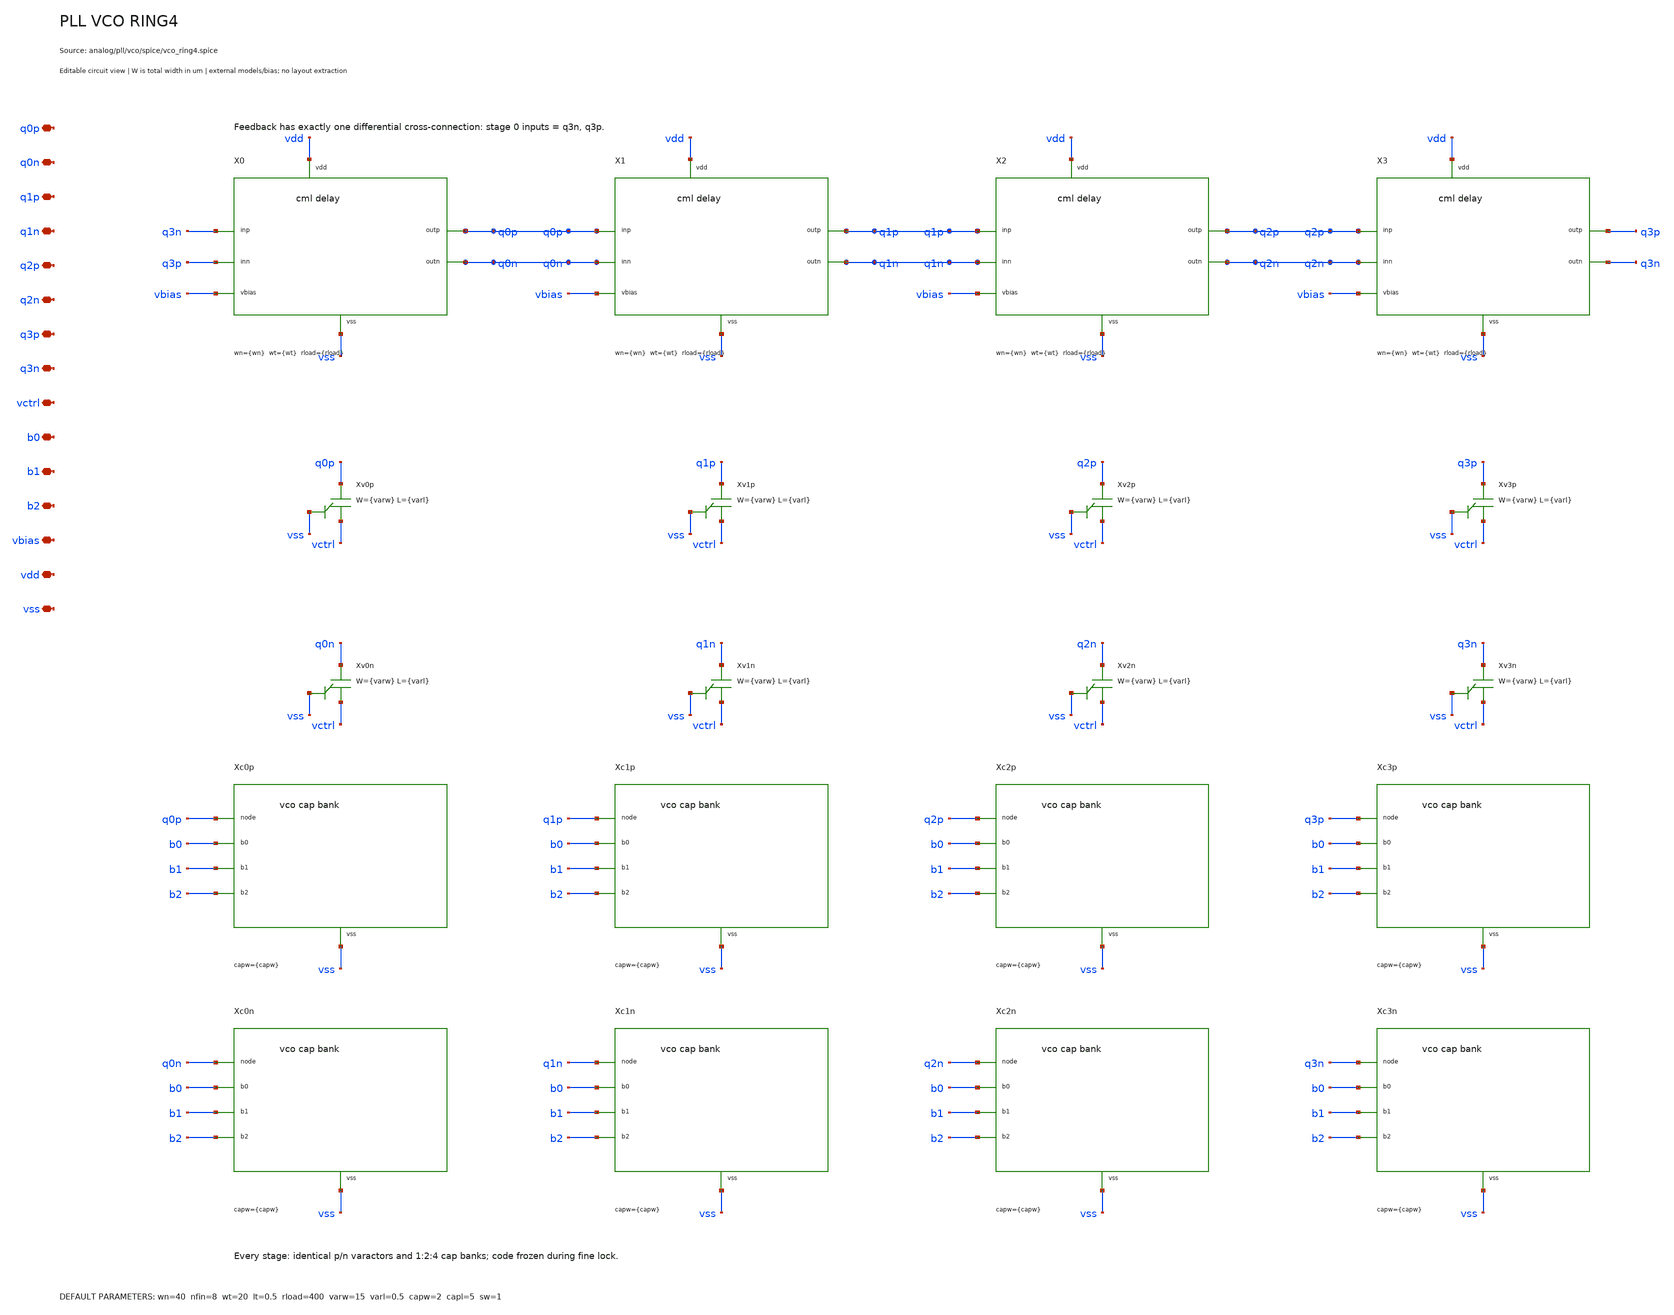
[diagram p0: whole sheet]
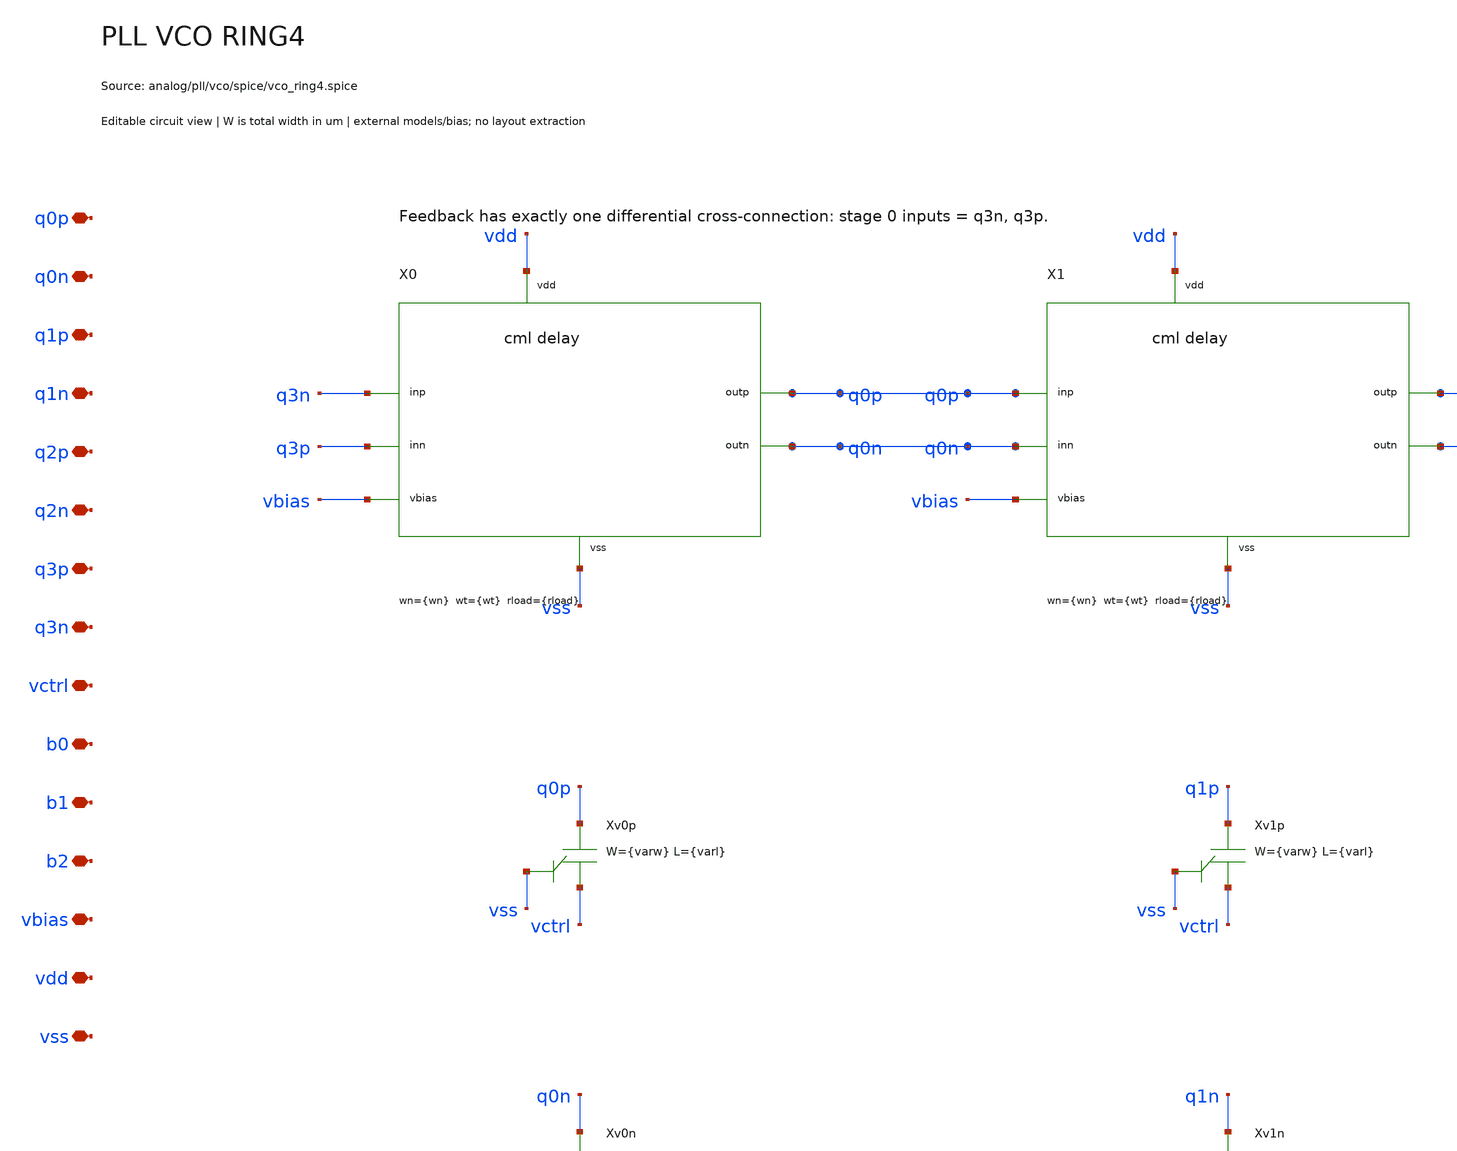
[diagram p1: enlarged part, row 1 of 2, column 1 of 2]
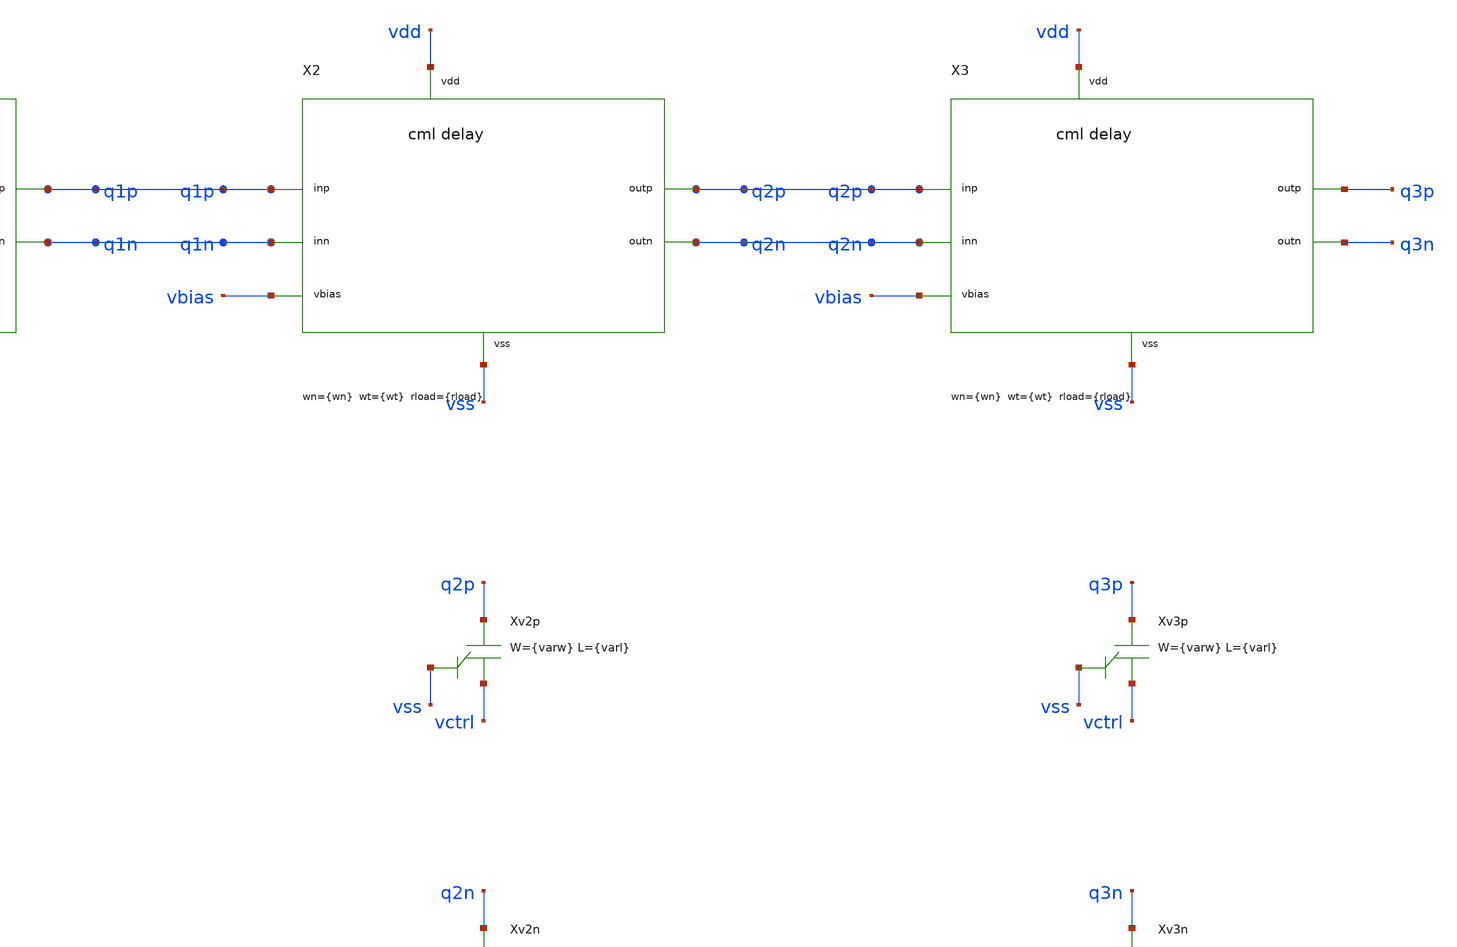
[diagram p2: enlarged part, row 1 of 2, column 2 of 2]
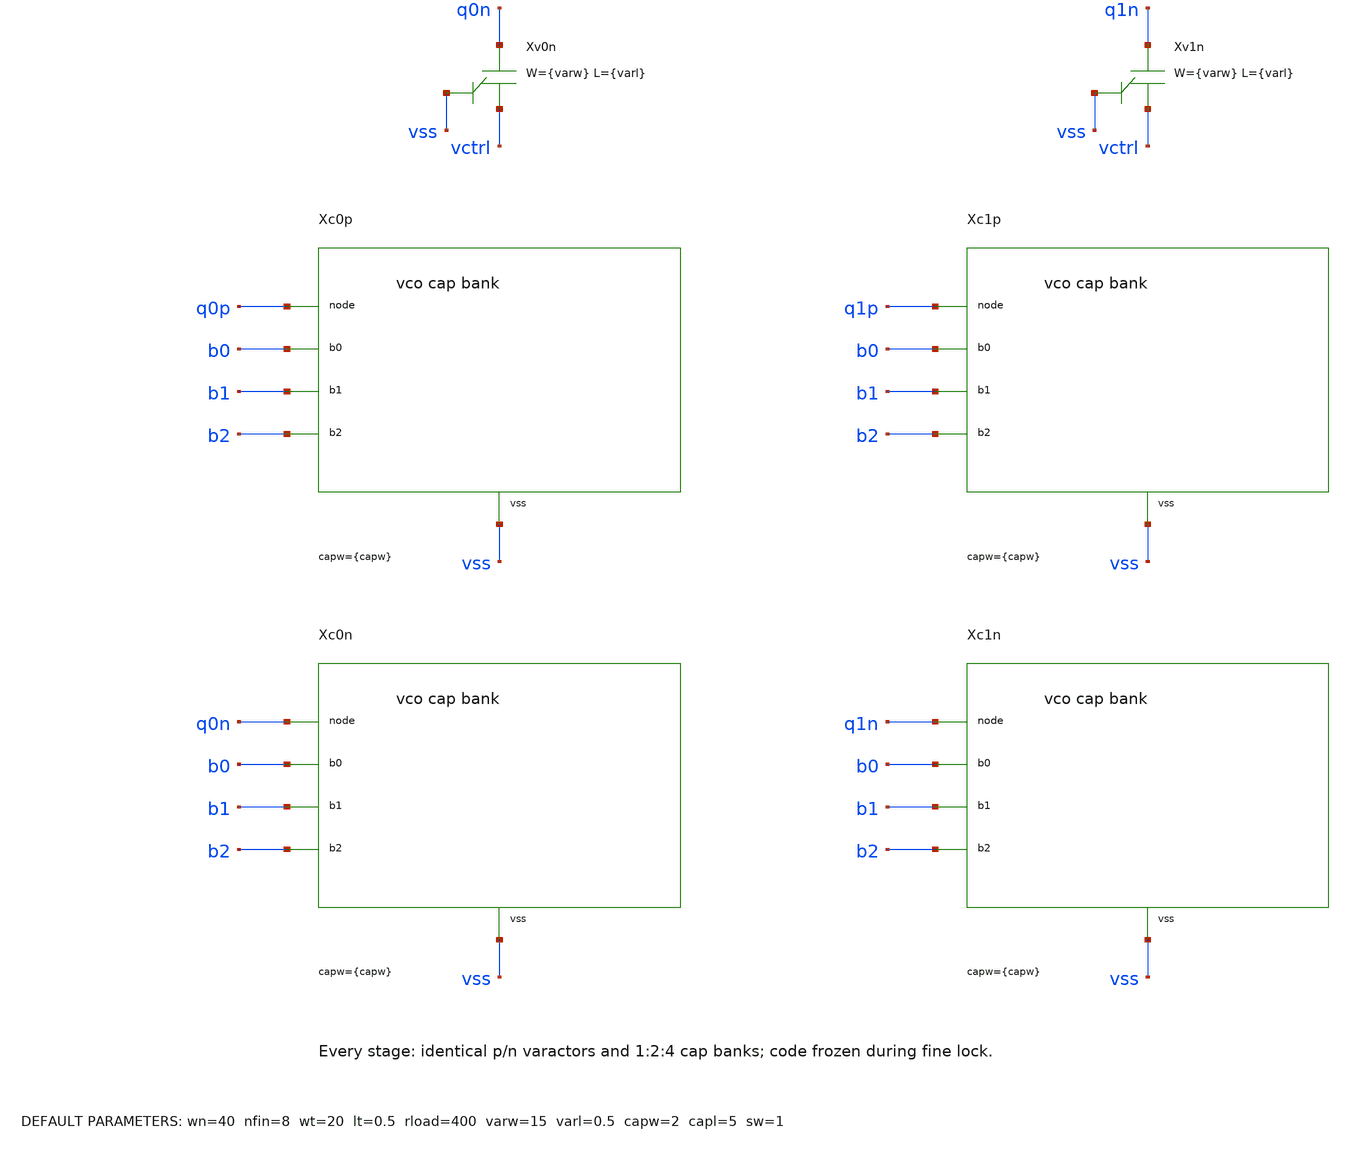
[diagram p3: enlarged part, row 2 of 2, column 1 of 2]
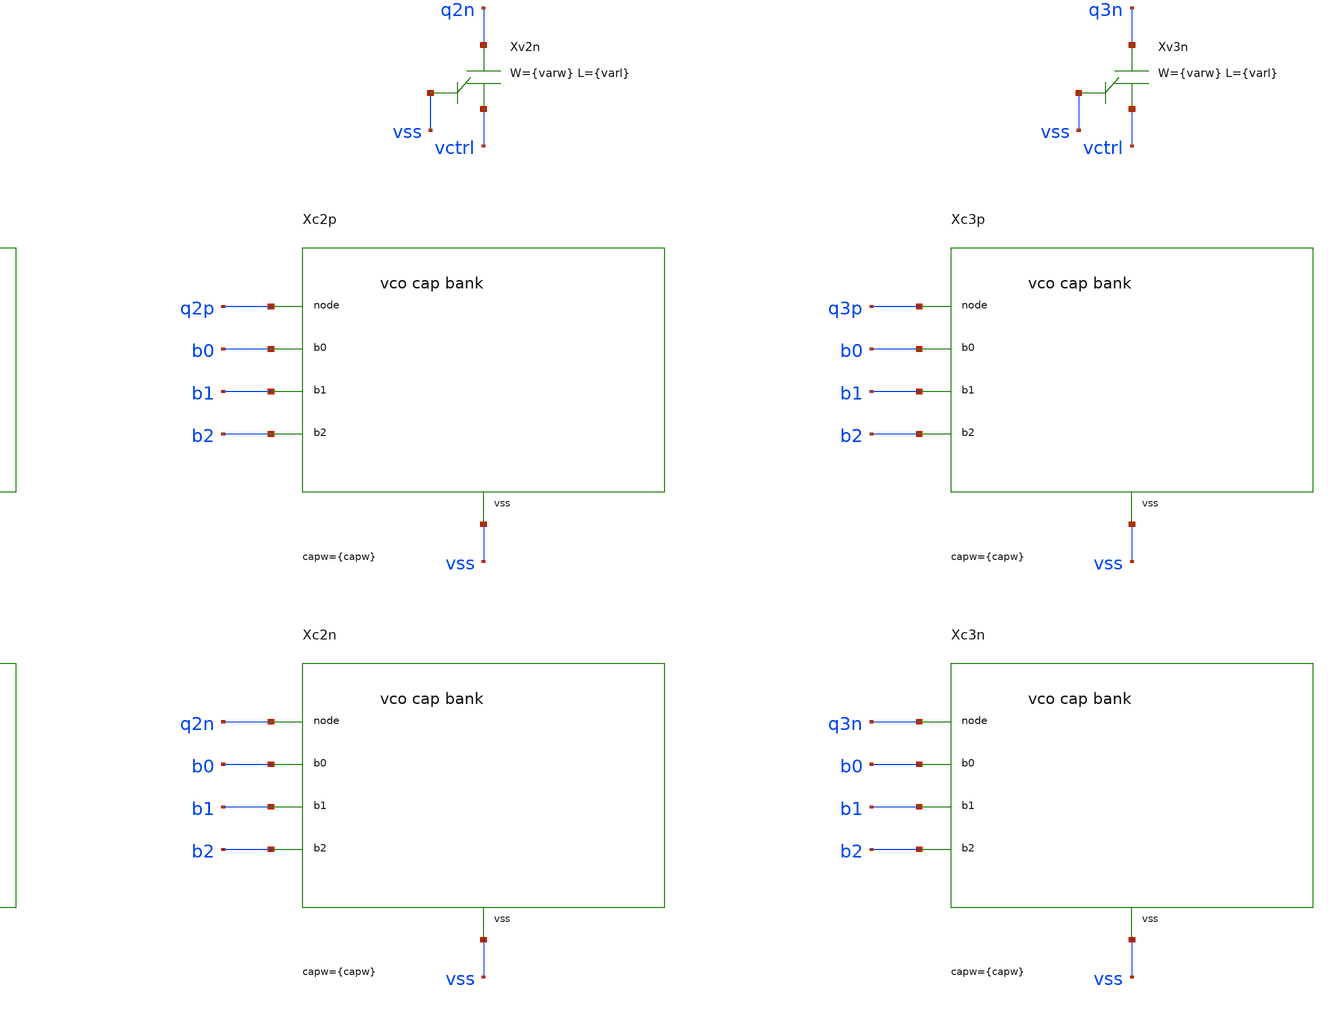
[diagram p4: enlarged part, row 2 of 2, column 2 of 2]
** sch_path: analog/pll/vco/schematic/pll_vco_ring4.sch
**.subckt pll_vco_ring4 q0p q0n q1p q1n q2p q2n q3p q3n vctrl b0 b1 b2 vbias vdd vss
*.iopin q0p
*.iopin q0n
*.iopin q1p
*.iopin q1n
*.iopin q2p
*.iopin q2n
*.iopin q3p
*.iopin q3n
*.iopin vctrl
*.iopin b0
*.iopin b1
*.iopin b2
*.iopin vbias
*.iopin vdd
*.iopin vss
X0 q3n q3p q0p q0n vbias vdd vss serdes_cml_delay wn={wn} lin=0.15 nfin={nfin} wt={wt} lt={lt} nftail=4
+ rload={rload}
X1 q0p q0n q1p q1n vbias vdd vss serdes_cml_delay wn={wn} lin=0.15 nfin={nfin} wt={wt} lt={lt} nftail=4
+ rload={rload}
X2 q1p q1n q2p q2n vbias vdd vss serdes_cml_delay wn={wn} lin=0.15 nfin={nfin} wt={wt} lt={lt} nftail=4
+ rload={rload}
X3 q2p q2n q3p q3n vbias vdd vss serdes_cml_delay wn={wn} lin=0.15 nfin={nfin} wt={wt} lt={lt} nftail=4
+ rload={rload}
Xv0p q0p vctrl vss sky130_fd_pr__cap_var_lvt w={varw} l={varl}
Xv0n q0n vctrl vss sky130_fd_pr__cap_var_lvt w={varw} l={varl}
Xv1p q1p vctrl vss sky130_fd_pr__cap_var_lvt w={varw} l={varl}
Xv1n q1n vctrl vss sky130_fd_pr__cap_var_lvt w={varw} l={varl}
Xv2p q2p vctrl vss sky130_fd_pr__cap_var_lvt w={varw} l={varl}
Xv2n q2n vctrl vss sky130_fd_pr__cap_var_lvt w={varw} l={varl}
Xv3p q3p vctrl vss sky130_fd_pr__cap_var_lvt w={varw} l={varl}
Xv3n q3n vctrl vss sky130_fd_pr__cap_var_lvt w={varw} l={varl}
Xc0p q0p b0 b1 b2 vss pll_vco_cap_bank capw={capw} capl={capl} sw={sw}
Xc0n q0n b0 b1 b2 vss pll_vco_cap_bank capw={capw} capl={capl} sw={sw}
Xc1p q1p b0 b1 b2 vss pll_vco_cap_bank capw={capw} capl={capl} sw={sw}
Xc1n q1n b0 b1 b2 vss pll_vco_cap_bank capw={capw} capl={capl} sw={sw}
Xc2p q2p b0 b1 b2 vss pll_vco_cap_bank capw={capw} capl={capl} sw={sw}
Xc2n q2n b0 b1 b2 vss pll_vco_cap_bank capw={capw} capl={capl} sw={sw}
Xc3p q3p b0 b1 b2 vss pll_vco_cap_bank capw={capw} capl={capl} sw={sw}
Xc3n q3n b0 b1 b2 vss pll_vco_cap_bank capw={capw} capl={capl} sw={sw}
**.ends

* expanding   symbol:  serdes/serdes_cml_delay.sym # of pins=7
** sym_path: analog/common/cml_buffer/schematic/serdes_cml_delay.sym
** sch_path: analog/common/cml_buffer/schematic/serdes_cml_delay.sch
.subckt serdes_cml_delay inp inn outp outn vbias vdd vss  wn=40 lin=0.15 nfin=8 wt=20 lt=0.5
+ nftail=4 rload=400
*.iopin inp
*.iopin inn
*.iopin outp
*.iopin outn
*.iopin vbias
*.iopin vdd
*.iopin vss
Rp vdd outp {rload}
Rn vdd outn {rload}
Xmp outp inp tail vss sky130_fd_pr__nfet_01v8_lvt w={wn} l={lin} nf={nfin} ad={floor((nfin+1)/2)*(wn/nfin)*0.29}
+ as={floor((nfin+2)/2)*(wn/nfin)*0.29} pd={2*floor((nfin+1)/2)*(wn/nfin+0.29)} ps={2*floor((nfin+2)/2)*(wn/nfin+0.29)}
Xmn outn inn tail vss sky130_fd_pr__nfet_01v8_lvt w={wn} l={lin} nf={nfin} ad={floor((nfin+1)/2)*(wn/nfin)*0.29}
+ as={floor((nfin+2)/2)*(wn/nfin)*0.29} pd={2*floor((nfin+1)/2)*(wn/nfin+0.29)} ps={2*floor((nfin+2)/2)*(wn/nfin+0.29)}
Xtail tail vbias vss vss sky130_fd_pr__nfet_01v8 w={wt} l={lt} nf={nftail} ad={floor((nftail+1)/2)*(wt/nftail)*0.29}
+ as={floor((nftail+2)/2)*(wt/nftail)*0.29} pd={2*floor((nftail+1)/2)*(wt/nftail+0.29)} ps={2*floor((nftail+2)/2)*(wt/nftail+0.29)}
.ends


* expanding   symbol:  serdes/pll_vco_cap_bank.sym # of pins=5
** sym_path: analog/pll/vco/schematic/pll_vco_cap_bank.sym
** sch_path: analog/pll/vco/schematic/pll_vco_cap_bank.sch
.subckt pll_vco_cap_bank node b0 b1 b2 vss  capw=2 capl=2 sw=1
*.iopin node
*.iopin b0
*.iopin b1
*.iopin b2
*.iopin vss
X00 node b0 vss pll_vco_cap_unit capw={capw} capl={capl} sw={sw}
X10 node b1 vss pll_vco_cap_unit capw={capw} capl={capl} sw={sw}
X11 node b1 vss pll_vco_cap_unit capw={capw} capl={capl} sw={sw}
X20 node b2 vss pll_vco_cap_unit capw={capw} capl={capl} sw={sw}
X21 node b2 vss pll_vco_cap_unit capw={capw} capl={capl} sw={sw}
X22 node b2 vss pll_vco_cap_unit capw={capw} capl={capl} sw={sw}
X23 node b2 vss pll_vco_cap_unit capw={capw} capl={capl} sw={sw}
.ends


* expanding   symbol:  serdes/pll_vco_cap_unit.sym # of pins=3
** sym_path: analog/pll/vco/schematic/pll_vco_cap_unit.sym
** sch_path: analog/pll/vco/schematic/pll_vco_cap_unit.sch
.subckt pll_vco_cap_unit node en vss  capw=2 capl=2 sw=1
*.iopin node
*.iopin en
*.iopin vss
Xcap node plate sky130_fd_pr__cap_mim_m3_1 w={capw} l={capl}
Xsw plate en vss vss sky130_fd_pr__nfet_01v8 w={sw} l=0.15 nf=1 ad={sw*0.29} as={sw*0.29} pd={2*(sw+0.29)}
+ ps={2*(sw+0.29)}
Rdc plate vss 1T
.ends

.end
